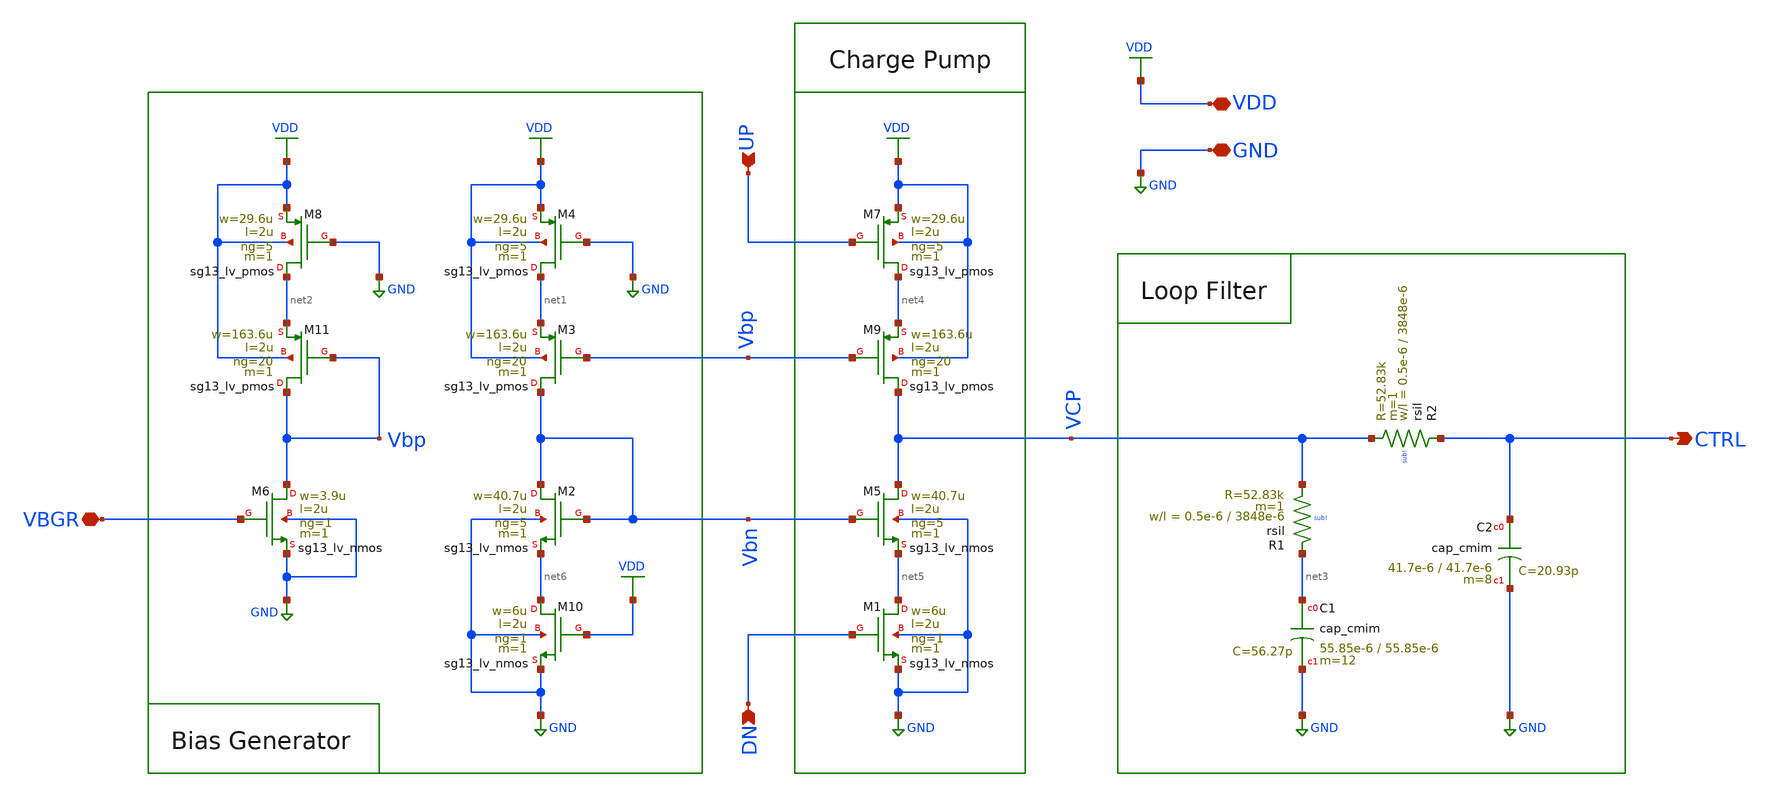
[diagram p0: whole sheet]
** sch_path: schematic/charge-pump/CP.sch
**.subckt CP CTRL UP VDD DN GND VBGR
*.opin CTRL
*.ipin UP
*.iopin VDD
*.ipin DN
*.iopin GND
*.iopin VBGR
XM2 Vbn Vbn net6 GND sg13_lv_nmos w=40.7u l=2u ng=5 m=1 mm_ok=1
XM8 net2 GND VDD VDD sg13_lv_pmos w=29.6u l=2u ng=5 m=1 mm_ok=1
XR2 CTRL VCP sub! rsil w=0.5e-6 l=3848e-6 m=1 mm_ok=1
XR1 net3 VCP sub! rsil w=0.5e-6 l=3848e-6 m=1 mm_ok=1
XC2 CTRL GND cap_cmim w=41.7e-6 l=41.7e-6 m=8 mm_ok=1
XC1 net3 GND cap_cmim w=55.85e-6 l=55.85e-6 m=12 mm_ok=1
XM11 Vbp Vbp net2 VDD sg13_lv_pmos w=163.6u l=2u ng=20 m=1 mm_ok=1
XM3 Vbn Vbp net1 VDD sg13_lv_pmos w=163.6u l=2u ng=20 m=1 mm_ok=1
XM4 net1 GND VDD VDD sg13_lv_pmos w=29.6u l=2u ng=5 m=1 mm_ok=1
XM7 net4 UP VDD VDD sg13_lv_pmos w=29.6u l=2u ng=5 m=1 mm_ok=1
XM9 VCP Vbp net4 VDD sg13_lv_pmos w=163.6u l=2u ng=20 m=1 mm_ok=1
XM10 net6 VDD GND GND sg13_lv_nmos w=6u l=2u ng=1 m=1 mm_ok=1
XM1 net5 DN GND GND sg13_lv_nmos w=6u l=2u ng=1 m=1 mm_ok=1
XM5 VCP Vbn net5 GND sg13_lv_nmos w=40.7u l=2u ng=5 m=1 mm_ok=1
XM6 Vbp VBGR GND GND sg13_lv_nmos w=3.9u l=2u ng=1 m=1 mm_ok=1
**.ends
.GLOBAL GND
.GLOBAL VDD
.end
